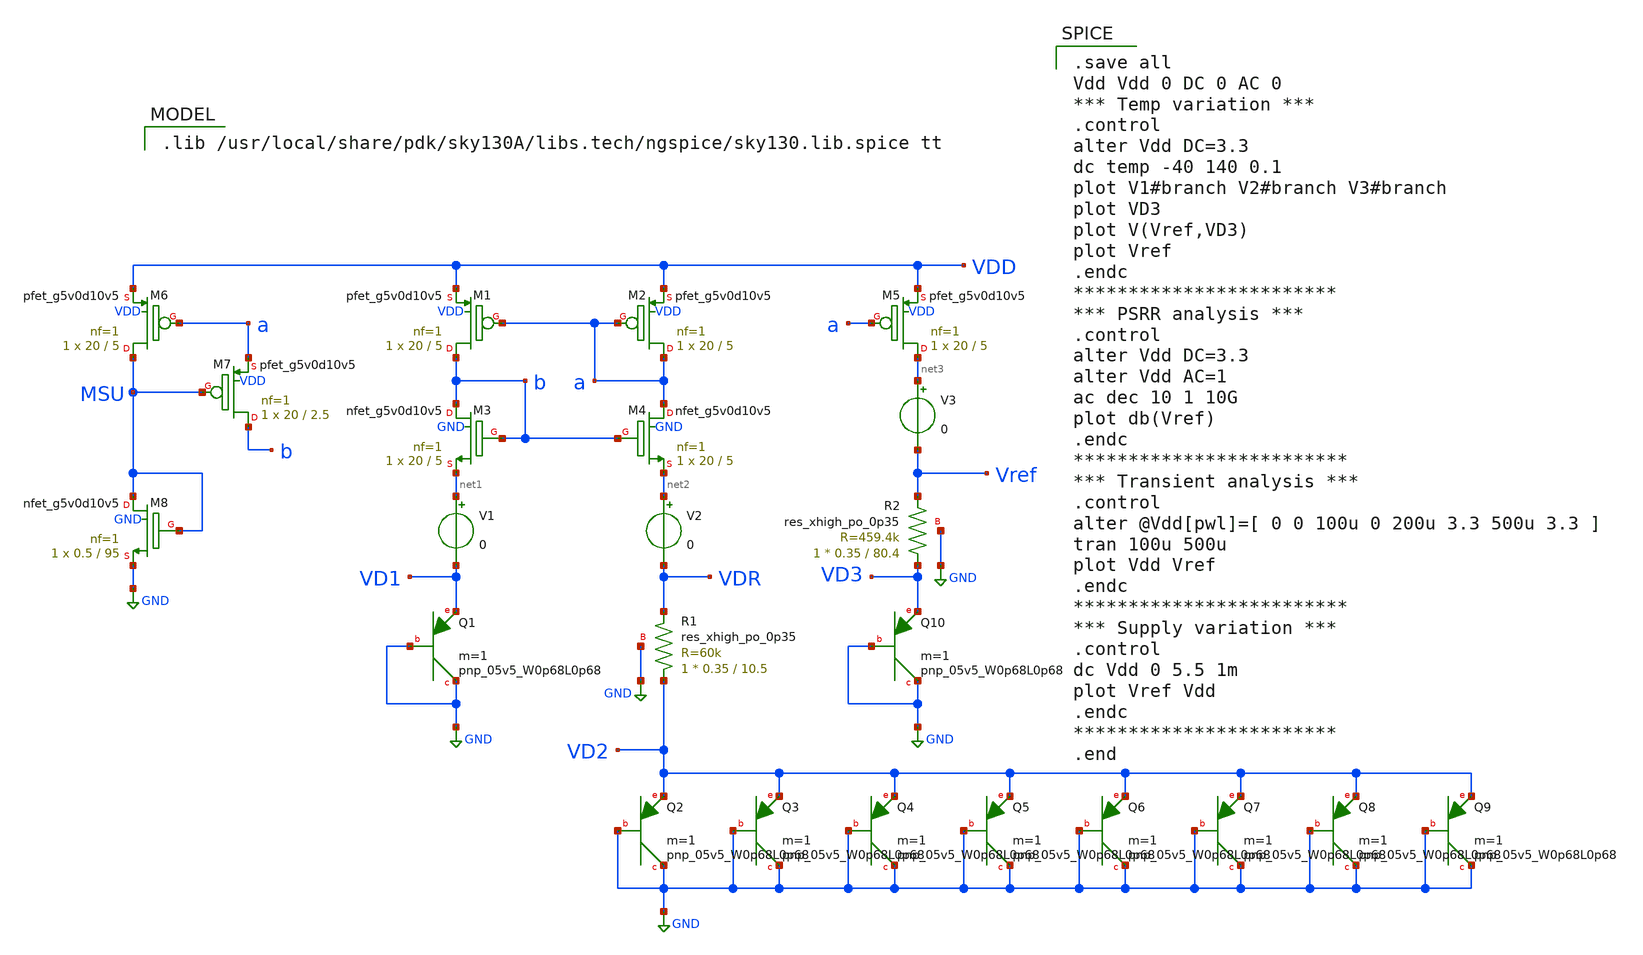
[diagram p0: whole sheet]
** sch_path: 2_BGR_nocas_0p68pnp.sch
**.subckt 2_BGR_nocas_0p68pnp
V1 net1 VD1 0
V2 net2 VDR 0
XQ2 GND GND VD2 sky130_fd_pr__pnp_05v5_W0p68L0p68 m=1
XQ3 GND GND VD2 sky130_fd_pr__pnp_05v5_W0p68L0p68 m=1
XQ4 GND GND VD2 sky130_fd_pr__pnp_05v5_W0p68L0p68 m=1
XQ5 GND GND VD2 sky130_fd_pr__pnp_05v5_W0p68L0p68 m=1
XQ6 GND GND VD2 sky130_fd_pr__pnp_05v5_W0p68L0p68 m=1
XQ7 GND GND VD2 sky130_fd_pr__pnp_05v5_W0p68L0p68 m=1
XQ8 GND GND VD2 sky130_fd_pr__pnp_05v5_W0p68L0p68 m=1
XQ9 GND GND VD2 sky130_fd_pr__pnp_05v5_W0p68L0p68 m=1
V3 net3 Vref 0
XQ1 GND GND VD1 sky130_fd_pr__pnp_05v5_W0p68L0p68 m=1
XQ10 GND GND VD3 sky130_fd_pr__pnp_05v5_W0p68L0p68 m=1
XR1 VD2 VDR GND sky130_fd_pr__res_xhigh_po_0p35 L=10.5 mult=1 m=1
XR2 VD3 Vref GND sky130_fd_pr__res_xhigh_po_0p35 L=80.4 mult=1 m=1
XM1 b a VDD VDD sky130_fd_pr__pfet_g5v0d10v5 L=5 W=20 nf=1 ad='int((nf+1)/2) * W/nf * 0.29' as='int((nf+2)/2) * W/nf * 0.29'
+ pd='2*int((nf+1)/2) * (W/nf + 0.29)' ps='2*int((nf+2)/2) * (W/nf + 0.29)' nrd='0.29 / W' nrs='0.29 / W'
+ sa=0 sb=0 sd=0 mult=1 m=1
XM2 a a VDD VDD sky130_fd_pr__pfet_g5v0d10v5 L=5 W=20 nf=1 ad='int((nf+1)/2) * W/nf * 0.29' as='int((nf+2)/2) * W/nf * 0.29'
+ pd='2*int((nf+1)/2) * (W/nf + 0.29)' ps='2*int((nf+2)/2) * (W/nf + 0.29)' nrd='0.29 / W' nrs='0.29 / W'
+ sa=0 sb=0 sd=0 mult=1 m=1
XM3 b b net1 GND sky130_fd_pr__nfet_g5v0d10v5 L=5 W=20 nf=1 ad='int((nf+1)/2) * W/nf * 0.29' as='int((nf+2)/2) * W/nf * 0.29'
+ pd='2*int((nf+1)/2) * (W/nf + 0.29)' ps='2*int((nf+2)/2) * (W/nf + 0.29)' nrd='0.29 / W' nrs='0.29 / W'
+ sa=0 sb=0 sd=0 mult=1 m=1
XM4 a b net2 GND sky130_fd_pr__nfet_g5v0d10v5 L=5 W=20 nf=1 ad='int((nf+1)/2) * W/nf * 0.29' as='int((nf+2)/2) * W/nf * 0.29'
+ pd='2*int((nf+1)/2) * (W/nf + 0.29)' ps='2*int((nf+2)/2) * (W/nf + 0.29)' nrd='0.29 / W' nrs='0.29 / W'
+ sa=0 sb=0 sd=0 mult=1 m=1
XM5 net3 a VDD VDD sky130_fd_pr__pfet_g5v0d10v5 L=5 W=20 nf=1 ad='int((nf+1)/2) * W/nf * 0.29' as='int((nf+2)/2) * W/nf * 0.29'
+ pd='2*int((nf+1)/2) * (W/nf + 0.29)' ps='2*int((nf+2)/2) * (W/nf + 0.29)' nrd='0.29 / W' nrs='0.29 / W'
+ sa=0 sb=0 sd=0 mult=1 m=1
XM6 MSU a VDD VDD sky130_fd_pr__pfet_g5v0d10v5 L=5 W=20 nf=1 ad='int((nf+1)/2) * W/nf * 0.29' as='int((nf+2)/2) * W/nf * 0.29'
+ pd='2*int((nf+1)/2) * (W/nf + 0.29)' ps='2*int((nf+2)/2) * (W/nf + 0.29)' nrd='0.29 / W' nrs='0.29 / W'
+ sa=0 sb=0 sd=0 mult=1 m=1
XM7 b MSU a VDD sky130_fd_pr__pfet_g5v0d10v5 L=2.5 W=20 nf=1 ad='int((nf+1)/2) * W/nf * 0.29' as='int((nf+2)/2) * W/nf * 0.29'
+ pd='2*int((nf+1)/2) * (W/nf + 0.29)' ps='2*int((nf+2)/2) * (W/nf + 0.29)' nrd='0.29 / W' nrs='0.29 / W'
+ sa=0 sb=0 sd=0 mult=1 m=1
XM8 MSU MSU GND GND sky130_fd_pr__nfet_g5v0d10v5 L=95 W=0.5 nf=1 ad='int((nf+1)/2) * W/nf * 0.29' as='int((nf+2)/2) * W/nf * 0.29'
+ pd='2*int((nf+1)/2) * (W/nf + 0.29)' ps='2*int((nf+2)/2) * (W/nf + 0.29)' nrd='0.29 / W' nrs='0.29 / W'
+ sa=0 sb=0 sd=0 mult=1 m=1
**** begin user architecture code

.lib /usr/local/share/pdk/sky130A/libs.tech/ngspice/sky130.lib.spice tt


.save all
Vdd Vdd 0 DC 0 AC 0
*** Temp variation ***
.control
alter Vdd DC=3.3
dc temp -40 140 0.1
plot V1#branch V2#branch V3#branch
plot VD3
plot V(Vref,VD3)
plot Vref
.endc
************************
*** PSRR analysis ***
.control
alter Vdd DC=3.3
alter Vdd AC=1
ac dec 10 1 10G
plot db(Vref)
.endc
*************************
*** Transient analysis ***
.control
alter @Vdd[pwl]=[ 0 0 100u 0 200u 3.3 500u 3.3 ]
tran 100u 500u
plot Vdd Vref
.endc
*************************
*** Supply variation ***
.control
dc Vdd 0 5.5 1m
plot Vref Vdd
.endc
************************
.end

**** end user architecture code
**.ends
.GLOBAL GND
.end
